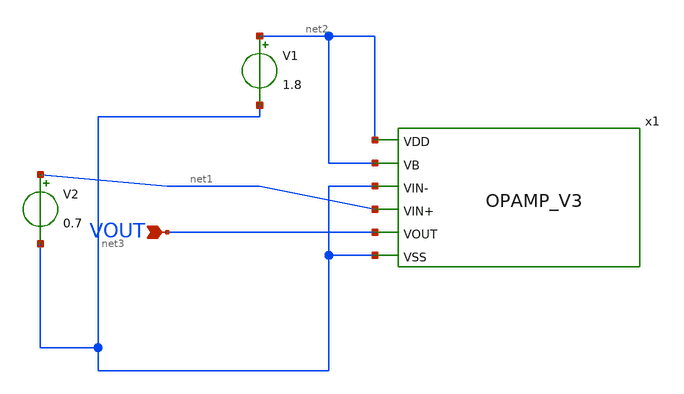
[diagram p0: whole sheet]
** sch_path: design/JNW_GR01_SKY130A/OPAMP_V4.sch
**.subckt OPAMP_V4 VOUT
*.ipin VOUT
V1 net2 net3 1.8
V2 net1 net3 0.7
x1 net2 net2 net3 net1 VOUT net3 OPAMP_V3
**.ends
.end
